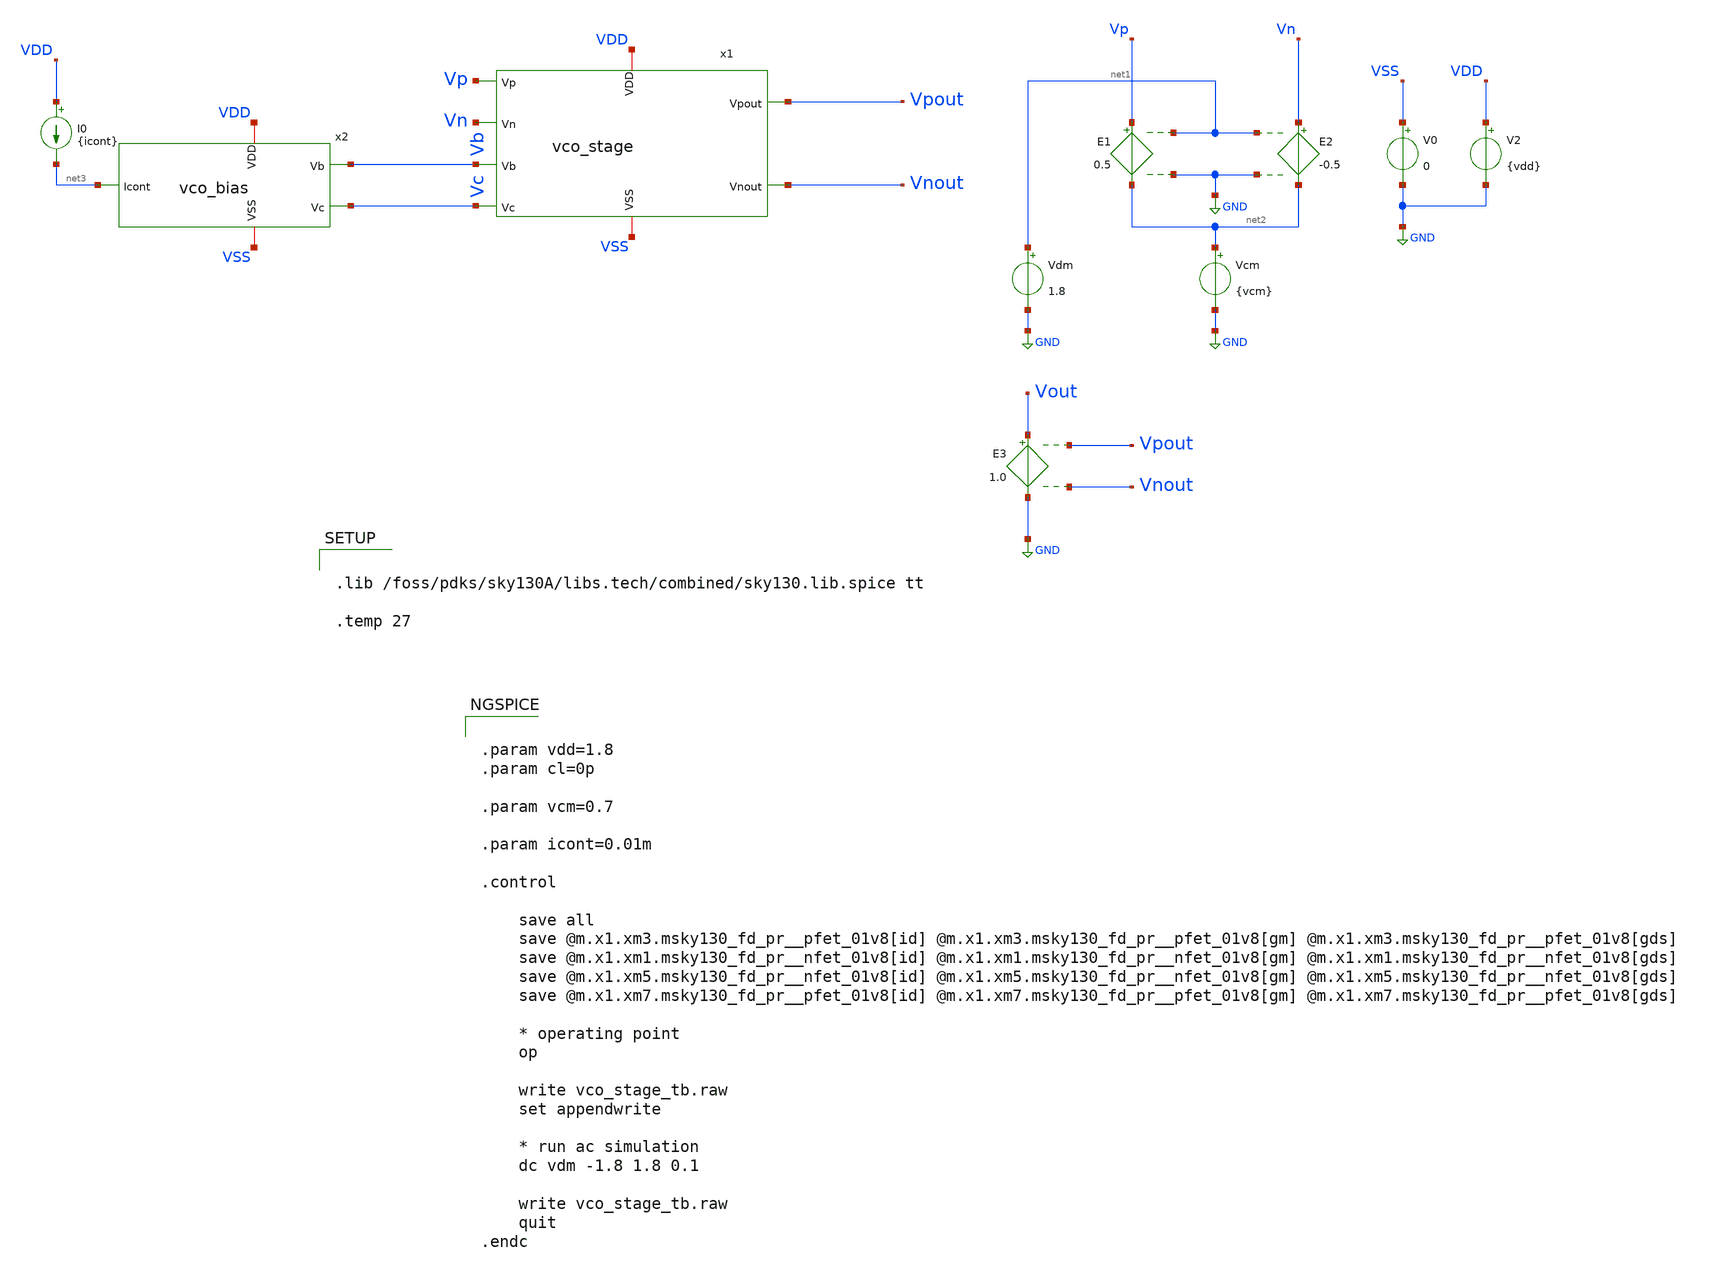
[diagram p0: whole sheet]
** sch_path: xschem/vco_stage_tb.sch
**.subckt vco_stage_tb
E1 Vp net2 net1 GND 0.5
E2 Vn net2 net1 GND -0.5
Vdm net1 GND 1.8
Vcm net2 GND {vcm}
V0 VSS GND 0
V2 VDD GND {vdd}
E3 Vout GND Vpout Vnout 1.0
x1 VDD VSS Vp Vn Vb Vc Vpout Vnout vco_stage
x2 VDD VSS net3 Vb Vc vco_bias
I0 VDD net3 {icont}
**** begin user architecture code


.param vdd=1.8
.param cl=0p

.param vcm=0.7

.param icont=0.01m

.control

    save all
    save @m.x1.xm3.msky130_fd_pr__pfet_01v8[id] @m.x1.xm3.msky130_fd_pr__pfet_01v8[gm]
+ @m.x1.xm3.msky130_fd_pr__pfet_01v8[gds]
    save @m.x1.xm1.msky130_fd_pr__nfet_01v8[id] @m.x1.xm1.msky130_fd_pr__nfet_01v8[gm]
+ @m.x1.xm1.msky130_fd_pr__nfet_01v8[gds]
    save @m.x1.xm5.msky130_fd_pr__nfet_01v8[id] @m.x1.xm5.msky130_fd_pr__nfet_01v8[gm]
+ @m.x1.xm5.msky130_fd_pr__nfet_01v8[gds]
    save @m.x1.xm7.msky130_fd_pr__pfet_01v8[id] @m.x1.xm7.msky130_fd_pr__pfet_01v8[gm]
+ @m.x1.xm7.msky130_fd_pr__pfet_01v8[gds]

    * operating point
    op

    write vco_stage_tb.raw
    set appendwrite

    * run ac simulation
    dc vdm -1.8 1.8 0.1

    write vco_stage_tb.raw
    quit
.endc




.lib /foss/pdks/sky130A/libs.tech/combined/sky130.lib.spice tt

.temp 27


**** end user architecture code
**.ends

* expanding   symbol:  vco_stage.sym # of pins=8
** sym_path: xschem/vco_stage.sym
** sch_path: xschem/vco_stage.sch
.subckt vco_stage VDD VSS Vp Vn Vb Vc Vpout Vnout
*.iopin VDD
*.iopin VSS
*.ipin Vp
*.ipin Vn
*.ipin Vb
*.ipin Vc
*.opin Vpout
*.opin Vnout
XM5 Vds_m5 Vc VSS VSS sky130_fd_pr__nfet_01v8 L={L} W={W} nf=2 ad='int((nf+1)/2) * W/nf * 0.29' as='int((nf+2)/2) * W/nf * 0.29'
+ pd='2*int((nf+1)/2) * (W/nf + 0.29)' ps='2*int((nf+2)/2) * (W/nf + 0.29)' nrd='0.29 / W' nrs='0.29 / W'
+ sa=0 sb=0 sd=0 mult=1 m=1
x1 VDD VSS Vp Vb Vnout Vpout Vds_m5 vco_stage_half
x2 VDD VSS Vn Vb Vpout Vnout Vds_m5 vco_stage_half
.ends


* expanding   symbol:  vco_bias.sym # of pins=5
** sym_path: xschem/vco_bias.sym
** sch_path: xschem/vco_bias.sch
.subckt vco_bias VDD VSS Icont Vb Vc
*.iopin VDD
*.iopin VSS
*.ipin Icont
*.opin Vb
*.opin Vc
XM1 Icont Icont VSS VSS sky130_fd_pr__nfet_01v8 L=1 W=2 nf=2 ad='int((nf+1)/2) * W/nf * 0.29' as='int((nf+2)/2) * W/nf * 0.29'
+ pd='2*int((nf+1)/2) * (W/nf + 0.29)' ps='2*int((nf+2)/2) * (W/nf + 0.29)' nrd='0.29 / W' nrs='0.29 / W'
+ sa=0 sb=0 sd=0 mult=1 m=1
XM2 Vb Icont VSS VSS sky130_fd_pr__nfet_01v8 L=1 W=2 nf=2 ad='int((nf+1)/2) * W/nf * 0.29' as='int((nf+2)/2) * W/nf * 0.29'
+ pd='2*int((nf+1)/2) * (W/nf + 0.29)' ps='2*int((nf+2)/2) * (W/nf + 0.29)' nrd='0.29 / W' nrs='0.29 / W'
+ sa=0 sb=0 sd=0 mult=1 m=1
XM3 VDD Vb Vb VDD sky130_fd_pr__nfet_01v8 L=1 W=2 nf=2 ad='int((nf+1)/2) * W/nf * 0.29' as='int((nf+2)/2) * W/nf * 0.29'
+ pd='2*int((nf+1)/2) * (W/nf + 0.29)' ps='2*int((nf+2)/2) * (W/nf + 0.29)' nrd='0.29 / W' nrs='0.29 / W'
+ sa=0 sb=0 sd=0 mult=1 m=1
V1 Vc Icont 0
.ends


* expanding   symbol:  vco_stage_half.sym # of pins=7
** sym_path: xschem/vco_stage_half.sym
** sch_path: xschem/vco_stage_half.sch
.subckt vco_stage_half VDD VSS Vin Vb Vd Vout Vs
*.iopin VDD
*.iopin VSS
*.ipin Vin
*.ipin Vb
*.ipin Vd
*.opin Vout
*.opin Vs
XM8 VSS Vout VSS VSS sky130_fd_pr__nfet_01v8 L={WLcap} W={WLcap} nf=1 ad='int((nf+1)/2) * W/nf * 0.29'
+ as='int((nf+2)/2) * W/nf * 0.29' pd='2*int((nf+1)/2) * (W/nf + 0.29)' ps='2*int((nf+2)/2) * (W/nf + 0.29)'
+ nrd='0.29 / W' nrs='0.29 / W' sa=0 sb=0 sd=0 mult=1 m=1
XM7 Vout Vd VDD VDD sky130_fd_pr__pfet_01v8 L={L} W={W} nf=2 ad='int((nf+1)/2) * W/nf * 0.29' as='int((nf+2)/2) * W/nf * 0.29'
+ pd='2*int((nf+1)/2) * (W/nf + 0.29)' ps='2*int((nf+2)/2) * (W/nf + 0.29)' nrd='0.29 / W' nrs='0.29 / W'
+ sa=0 sb=0 sd=0 mult=1 m=1
XM3 Vout Vb VDD VDD sky130_fd_pr__pfet_01v8 L={L} W={W} nf=2 ad='int((nf+1)/2) * W/nf * 0.29' as='int((nf+2)/2) * W/nf * 0.29'
+ pd='2*int((nf+1)/2) * (W/nf + 0.29)' ps='2*int((nf+2)/2) * (W/nf + 0.29)' nrd='0.29 / W' nrs='0.29 / W'
+ sa=0 sb=0 sd=0 mult=1 m=1
XM1 Vout Vin Vs VSS sky130_fd_pr__nfet_01v8 L={L} W={W} nf=2 ad='int((nf+1)/2) * W/nf * 0.29' as='int((nf+2)/2) * W/nf * 0.29'
+ pd='2*int((nf+1)/2) * (W/nf + 0.29)' ps='2*int((nf+2)/2) * (W/nf + 0.29)' nrd='0.29 / W' nrs='0.29 / W'
+ sa=0 sb=0 sd=0 mult=1 m=1
.ends

.GLOBAL GND
.end
